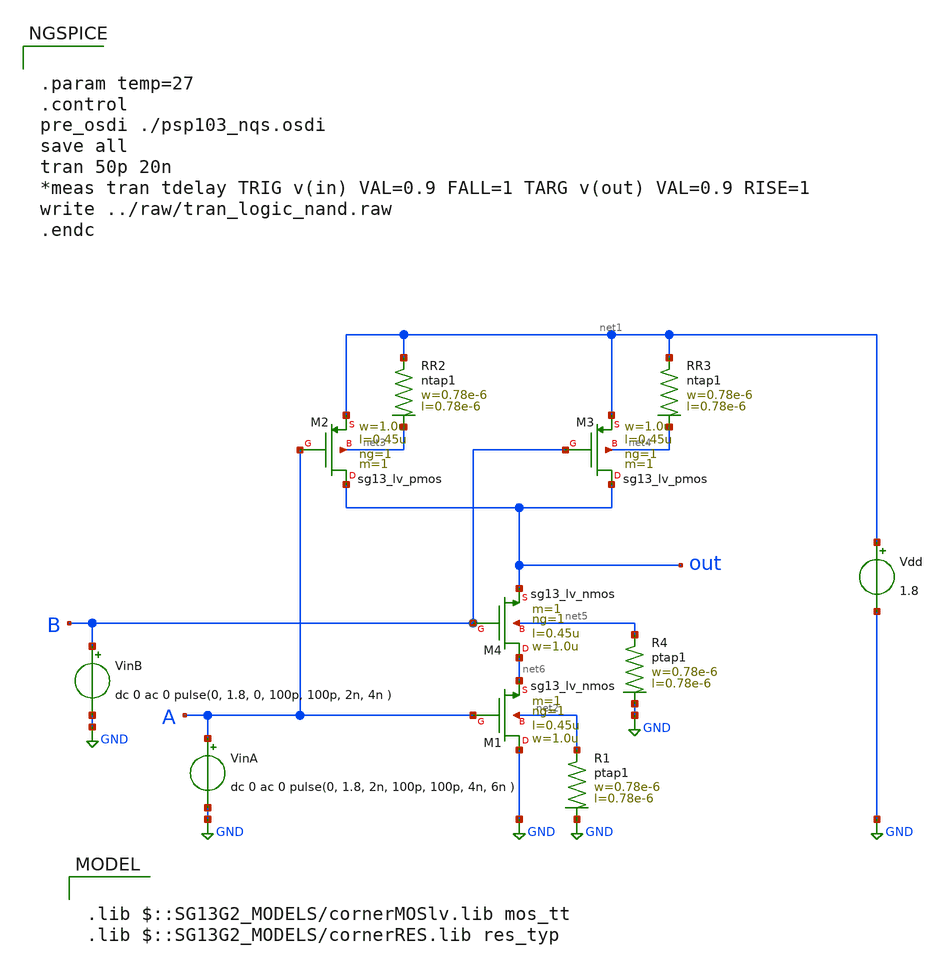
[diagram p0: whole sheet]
** sch_path: ihp-sg13g2/libs.tech/xschem/sg13g2_tests/tran_logic_nand.sch
* Copyright 2023 IHP PDK Authors
**.subckt tran_logic_nand
VinA A GND dc 0 ac 0 pulse(0, 1.8, 2n, 100p, 100p, 4n, 6n )
Vdd net1 GND 1.8
XM1 GND A net6 net2 sg13_lv_nmos w=1.0u l=0.45u ng=1 m=1 mm_ok=1
XR1 net2 GND ptap1 R=262.8 w=0.78e-6 l=0.78e-6
XR2 net1 net3 ntap1 R=262.8 w=0.78e-6 l=0.78e-6
XM2 out A net1 net3 sg13_lv_pmos w=1.0u l=0.45u ng=1 m=1 mm_ok=1
XR3 net1 net4 ntap1 R=262.8 w=0.78e-6 l=0.78e-6
XM3 out B net1 net4 sg13_lv_pmos w=1.0u l=0.45u ng=1 m=1 mm_ok=1
XM4 net6 B out net5 sg13_lv_nmos w=1.0u l=0.45u ng=1 m=1 mm_ok=1
XR4 net5 GND ptap1 R=262.8 w=0.78e-6 l=0.78e-6
VinB B GND dc 0 ac 0 pulse(0, 1.8, 0, 100p, 100p, 2n, 4n )
**** begin user architecture code

.lib $::SG13G2_MODELS/cornerMOSlv.lib mos_tt
.lib $::SG13G2_MODELS/cornerRES.lib res_typ



.param temp=27
.control
pre_osdi ./psp103_nqs.osdi
save all
tran 50p 20n
*meas tran tdelay TRIG v(in) VAL=0.9 FALL=1 TARG v(out) VAL=0.9 RISE=1
write ../raw/tran_logic_nand.raw
.endc


**** end user architecture code
**.ends
.GLOBAL GND
.end
